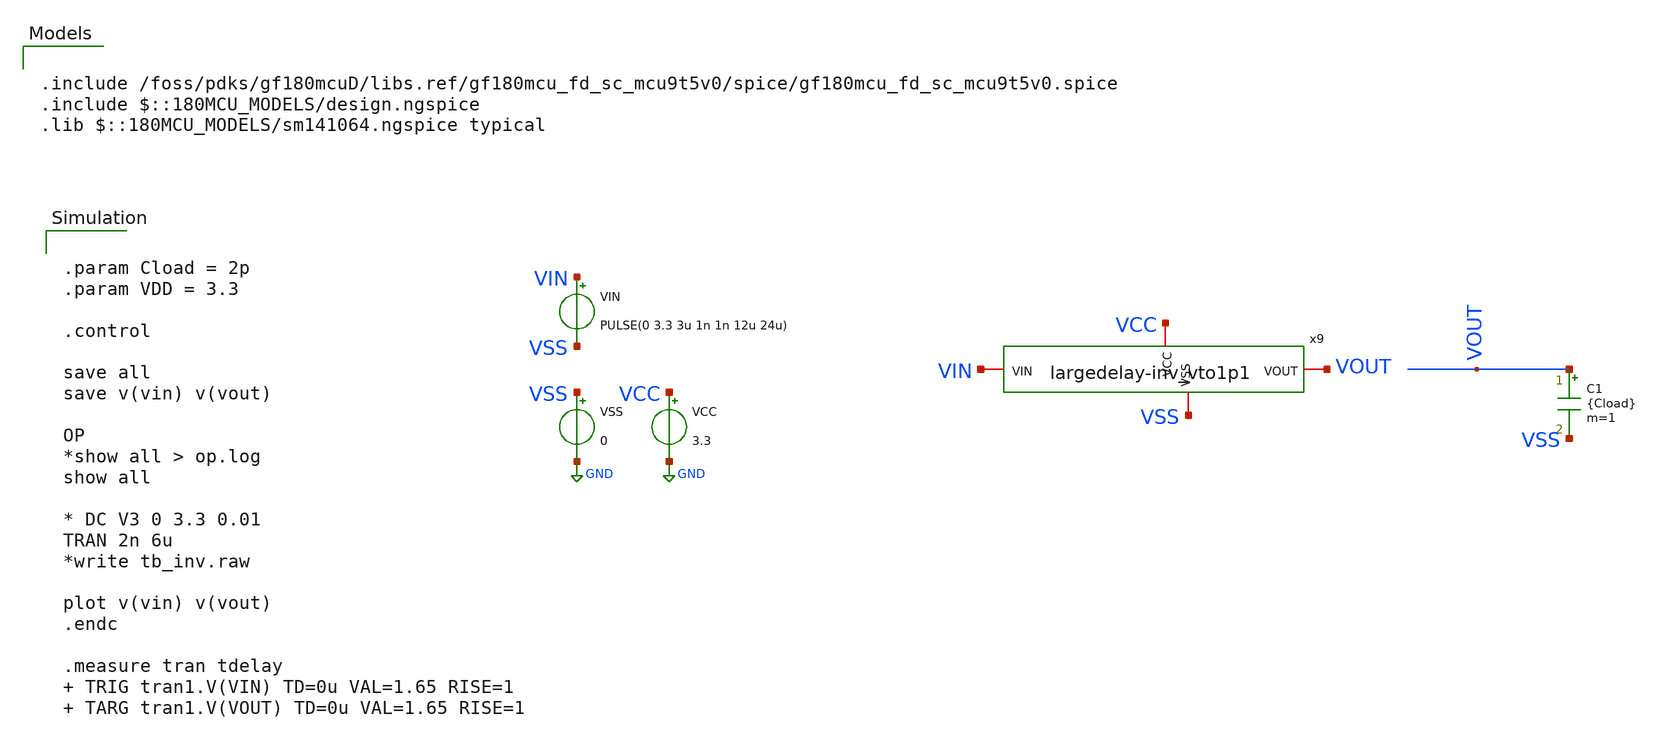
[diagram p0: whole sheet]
** sch_path: xschem/large_delay/tb_largedelay-inv_vto2p1.sch
**.subckt tb_largedelay-inv_vto2p1
VCC VCC GND 3.3
VSS VSS GND 0
VIN VIN VSS PULSE(0 3.3 3u 1n 1n 12u 24u)
C1 VOUT VSS {Cload} m=1
x9 VCC VSS VIN VOUT largedelay-inv_vto1p1
**** begin user architecture code


.param Cload = 2p
.param VDD = 3.3

.control

save all
save v(vin) v(vout)

OP
*show all > op.log
show all

* DC V3 0 3.3 0.01
TRAN 2n 6u
*write tb_inv.raw

plot v(vin) v(vout)
.endc

.measure tran tdelay  TRIG tran1.V(VIN) TD=0u VAL=1.65 RISE=1  TARG tran1.V(VOUT) TD=0u VAL=1.65
+ RISE=1



.include /foss/pdks/gf180mcuD/libs.ref/gf180mcu_fd_sc_mcu9t5v0/spice/gf180mcu_fd_sc_mcu9t5v0.spice
.include $::180MCU_MODELS/design.ngspice
.lib $::180MCU_MODELS/sm141064.ngspice typical

**** end user architecture code
**.ends

* expanding   symbol:  largedelay-inv_vto1p1.sym # of pins=4
** sym_path: xschem/large_delay/largedelay-inv_vto1p1.sym
** sch_path: xschem/large_delay/largedelay-inv_vto1p1.sch
.subckt largedelay-inv_vto1p1 VCC VSS VIN VOUT
*.iopin VIN
*.iopin VOUT
*.iopin VCC
*.iopin VSS
x1[0] VIN VSS VCC VSS VCC n2 gf180mcu_fd_sc_mcu9t5v0__inv_1
x1[1] n2 VSS VCC VSS VCC n3 gf180mcu_fd_sc_mcu9t5v0__inv_1
x1[2] n3 VSS VCC VSS VCC n4 gf180mcu_fd_sc_mcu9t5v0__inv_1
x1[3] n4 VSS VCC VSS VCC n5 gf180mcu_fd_sc_mcu9t5v0__inv_1
x1[4] n5 VSS VCC VSS VCC n6 gf180mcu_fd_sc_mcu9t5v0__inv_1
x1[5] n6 VSS VCC VSS VCC VOUT gf180mcu_fd_sc_mcu9t5v0__inv_1
.ends

.GLOBAL GND
.end
